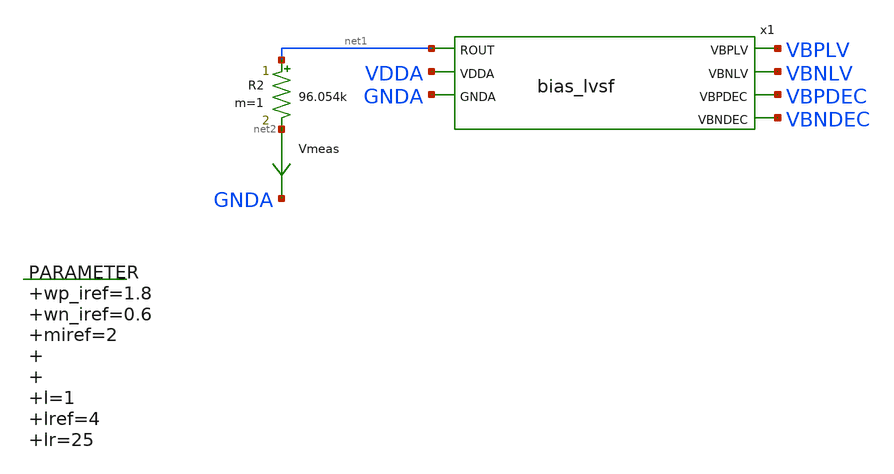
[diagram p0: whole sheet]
** sch_path: xschem/bias_lvsf-tb.sch
.lib $::SKYWATER_MODELS/sky130.lib.spice tt
.include $::SKYWATER_STDCELLS/sky130_fd_sc_hd.spice

**.subckt bias_lvsf-tb
.param wp_iref=1.8 wn_iref=0.6 miref=2 l=1 lref=4 lr=25
R2 net1 net2 96.054k m=1
Vmeas net2 GNDA 0
.save i(vmeas)
x1 net1 VBPLV VBNLV VBPDEC VBNDEC VDDA GNDA bias_lvsf
**** begin user architecture code



  .option wnflag=1
  .option safecurrents
  ***************************STATIC VOLTAGE SOURCE****************************
  Vddh vdda gnd dc 5.5
  VGNDA GNDA gnd 0
  **************************PARAMETERS****************************************
  *.param wsn1=0.6 wsn2=0.6 lx1=5.3 lx2=9.7 lx3=9.2 lx4=4 ws3=1 ws4=1 wsn3=0.64 lx5=12
  .dc R2 80k 120k 1k
  .control
     reset
     save all
     write bias_lvsf-tb.raw
     set wr_singlescale
     set wr_vecnames
     compose wsn1_vec start=0.6 stop=2 step=0.1
     compose wsn2_vec start=0.6 stop=0.7 step=0.01
     compose lx1_vec start=8 stop=15 step=0.1

     *foreach var1 $&wsn2_vec
       *alterparam wsn2=$var1
       reset
       save all
       run
       write bias_lvsf-tb.raw
       set appendwrite
     *end
*    quit 0
  .endc



**** end user architecture code
**.ends

* expanding   symbol:  bias_lvsf.sym # of pins=7
** sym_path: xschem/bias_lvsf.sym
** sch_path: xschem/bias_lvsf.sch
.subckt bias_lvsf ROUT VBPLV VBNLV VBPDEC VBNDEC VDDA GNDA
*.ipin ROUT
*.opin VBPLV
*.opin VBNLV
*.opin VBPDEC
*.opin VBNDEC
*.ipin VDDA
*.ipin GNDA
XM1 n1 n1 VDDA VDDA sky130_fd_pr__pfet_g5v0d10v5 L=lref W=wp_iref nf=1 ad='int((nf+1)/2) * W/nf * 0.29'
+ as='int((nf+2)/2) * W/nf * 0.29' pd='2*int((nf+1)/2) * (W/nf + 0.29)' ps='2*int((nf+2)/2) * (W/nf + 0.29)'
+ nrd='0.29 / W' nrs='0.29 / W' sa=0 sb=0 sd=0 mult=miref m=miref
.param wp_iref=1.8 wn_iref=0.6 miref=2 lref=4 lr=25
XM2 n2 n2 n1 VDDA sky130_fd_pr__pfet_g5v0d10v5 L=lref W=wp_iref nf=1 ad='int((nf+1)/2) * W/nf * 0.29'
+ as='int((nf+2)/2) * W/nf * 0.29' pd='2*int((nf+1)/2) * (W/nf + 0.29)' ps='2*int((nf+2)/2) * (W/nf + 0.29)'
+ nrd='0.29 / W' nrs='0.29 / W' sa=0 sb=0 sd=0 mult=miref m=miref
XR1 ROUT net1 GNDA sky130_fd_pr__res_xhigh_po_5p73 L=0.573 mult=1 m=1
XM3 net2 net1 n2 VDDA sky130_fd_pr__pfet_g5v0d10v5 L=lr W=wp_iref nf=1 ad='int((nf+1)/2) * W/nf * 0.29'
+ as='int((nf+2)/2) * W/nf * 0.29' pd='2*int((nf+1)/2) * (W/nf + 0.29)' ps='2*int((nf+2)/2) * (W/nf + 0.29)'
+ nrd='0.29 / W' nrs='0.29 / W' sa=0 sb=0 sd=0 mult=miref m=miref
XM4 net1 net1 net2 VDDA sky130_fd_pr__pfet_g5v0d10v5 L=lr W=wp_iref nf=1 ad='int((nf+1)/2) * W/nf * 0.29'
+ as='int((nf+2)/2) * W/nf * 0.29' pd='2*int((nf+1)/2) * (W/nf + 0.29)' ps='2*int((nf+2)/2) * (W/nf + 0.29)'
+ nrd='0.29 / W' nrs='0.29 / W' sa=0 sb=0 sd=0 mult=miref m=miref
XM5 net3 n1 VDDA VDDA sky130_fd_pr__pfet_g5v0d10v5 L=lref W=wp_iref nf=1 ad='int((nf+1)/2) * W/nf * 0.29'
+ as='int((nf+2)/2) * W/nf * 0.29' pd='2*int((nf+1)/2) * (W/nf + 0.29)' ps='2*int((nf+2)/2) * (W/nf + 0.29)'
+ nrd='0.29 / W' nrs='0.29 / W' sa=0 sb=0 sd=0 mult=miref m=miref
XM6 n3 n2 net3 VDDA sky130_fd_pr__pfet_g5v0d10v5 L=lref W=wp_iref nf=1 ad='int((nf+1)/2) * W/nf * 0.29'
+ as='int((nf+2)/2) * W/nf * 0.29' pd='2*int((nf+1)/2) * (W/nf + 0.29)' ps='2*int((nf+2)/2) * (W/nf + 0.29)'
+ nrd='0.29 / W' nrs='0.29 / W' sa=0 sb=0 sd=0 mult=miref m=miref
Vmeas1 net8 GNDA 0
.save i(vmeas1)
XM7 n3 n3 n4 GNDA sky130_fd_pr__nfet_g5v0d10v5 L=lref W=wn_iref nf=1 ad='int((nf+1)/2) * W/nf * 0.29'
+ as='int((nf+2)/2) * W/nf * 0.29' pd='2*int((nf+1)/2) * (W/nf + 0.29)' ps='2*int((nf+2)/2) * (W/nf + 0.29)'
+ nrd='0.29 / W' nrs='0.29 / W' sa=0 sb=0 sd=0 mult=miref m=miref
XM8 n4 n4 net8 GNDA sky130_fd_pr__nfet_g5v0d10v5 L=lref W=wn_iref nf=1 ad='int((nf+1)/2) * W/nf * 0.29'
+ as='int((nf+2)/2) * W/nf * 0.29' pd='2*int((nf+1)/2) * (W/nf + 0.29)' ps='2*int((nf+2)/2) * (W/nf + 0.29)'
+ nrd='0.29 / W' nrs='0.29 / W' sa=0 sb=0 sd=0 mult=miref m=miref
XM9 net4 n1 VDDA VDDA sky130_fd_pr__pfet_g5v0d10v5 L=lref W=wp_iref nf=1 ad='int((nf+1)/2) * W/nf * 0.29'
+ as='int((nf+2)/2) * W/nf * 0.29' pd='2*int((nf+1)/2) * (W/nf + 0.29)' ps='2*int((nf+2)/2) * (W/nf + 0.29)'
+ nrd='0.29 / W' nrs='0.29 / W' sa=0 sb=0 sd=0 mult=miref m=miref
XM10 VBNLV n2 net4 VDDA sky130_fd_pr__pfet_g5v0d10v5 L=lref W=wp_iref nf=1 ad='int((nf+1)/2) * W/nf * 0.29'
+ as='int((nf+2)/2) * W/nf * 0.29' pd='2*int((nf+1)/2) * (W/nf + 0.29)' ps='2*int((nf+2)/2) * (W/nf + 0.29)'
+ nrd='0.29 / W' nrs='0.29 / W' sa=0 sb=0 sd=0 mult=miref m=miref
XM11 net5 n1 VDDA VDDA sky130_fd_pr__pfet_g5v0d10v5 L=lref W=wp_iref nf=1 ad='int((nf+1)/2) * W/nf * 0.29'
+ as='int((nf+2)/2) * W/nf * 0.29' pd='2*int((nf+1)/2) * (W/nf + 0.29)' ps='2*int((nf+2)/2) * (W/nf + 0.29)'
+ nrd='0.29 / W' nrs='0.29 / W' sa=0 sb=0 sd=0 mult=miref m=miref
XM12 VBNDEC n2 net5 VDDA sky130_fd_pr__pfet_g5v0d10v5 L=lref W=wp_iref nf=1 ad='int((nf+1)/2) * W/nf * 0.29'
+ as='int((nf+2)/2) * W/nf * 0.29' pd='2*int((nf+1)/2) * (W/nf + 0.29)' ps='2*int((nf+2)/2) * (W/nf + 0.29)'
+ nrd='0.29 / W' nrs='0.29 / W' sa=0 sb=0 sd=0 mult=miref m=miref
XM13 VBNLV VBNLV n6 GNDA sky130_fd_pr__nfet_g5v0d10v5 L=lref W=wn_iref nf=1 ad='int((nf+1)/2) * W/nf * 0.29'
+ as='int((nf+2)/2) * W/nf * 0.29' pd='2*int((nf+1)/2) * (W/nf + 0.29)' ps='2*int((nf+2)/2) * (W/nf + 0.29)'
+ nrd='0.29 / W' nrs='0.29 / W' sa=0 sb=0 sd=0 mult=miref m=miref
XM14 n6 VBNLV net9 GNDA sky130_fd_pr__nfet_g5v0d10v5 L=5.3 W=0.6 nf=1 ad='int((nf+1)/2) * W/nf * 0.29'
+ as='int((nf+2)/2) * W/nf * 0.29' pd='2*int((nf+1)/2) * (W/nf + 0.29)' ps='2*int((nf+2)/2) * (W/nf + 0.29)'
+ nrd='0.29 / W' nrs='0.29 / W' sa=0 sb=0 sd=0 mult=1 m=1
Vmeas2 net9 GNDA 0
.save i(vmeas2)
XM15 VBNDEC VBNDEC n7 GNDA sky130_fd_pr__nfet_g5v0d10v5 L=lref W=wn_iref nf=1 ad='int((nf+1)/2) * W/nf * 0.29'
+ as='int((nf+2)/2) * W/nf * 0.29' pd='2*int((nf+1)/2) * (W/nf + 0.29)' ps='2*int((nf+2)/2) * (W/nf + 0.29)'
+ nrd='0.29 / W' nrs='0.29 / W' sa=0 sb=0 sd=0 mult=miref m=miref
XM16 n7 VBNDEC net10 GNDA sky130_fd_pr__nfet_g5v0d10v5 L=9.7 W=0.61 nf=1 ad='int((nf+1)/2) * W/nf * 0.29'
+ as='int((nf+2)/2) * W/nf * 0.29' pd='2*int((nf+1)/2) * (W/nf + 0.29)' ps='2*int((nf+2)/2) * (W/nf + 0.29)'
+ nrd='0.29 / W' nrs='0.29 / W' sa=0 sb=0 sd=0 mult=1 m=1
Vmeas3 net10 GNDA 0
.save i(vmeas3)
XM17 n10 VBPLV VDDA VDDA sky130_fd_pr__pfet_g5v0d10v5 L=9.2 W=1 nf=1 ad='int((nf+1)/2) * W/nf * 0.29'
+ as='int((nf+2)/2) * W/nf * 0.29' pd='2*int((nf+1)/2) * (W/nf + 0.29)' ps='2*int((nf+2)/2) * (W/nf + 0.29)'
+ nrd='0.29 / W' nrs='0.29 / W' sa=0 sb=0 sd=0 mult=1 m=1
XM18 VBPLV VBPLV n10 VDDA sky130_fd_pr__pfet_g5v0d10v5 L=lref W=wp_iref nf=1 ad='int((nf+1)/2) * W/nf * 0.29'
+ as='int((nf+2)/2) * W/nf * 0.29' pd='2*int((nf+1)/2) * (W/nf + 0.29)' ps='2*int((nf+2)/2) * (W/nf + 0.29)'
+ nrd='0.29 / W' nrs='0.29 / W' sa=0 sb=0 sd=0 mult=miref m=miref
Vmeas4 net11 GNDA 0
.save i(vmeas4)
XM19 VBPLV n3 net6 GNDA sky130_fd_pr__nfet_g5v0d10v5 L=lref W=wn_iref nf=1 ad='int((nf+1)/2) * W/nf * 0.29'
+ as='int((nf+2)/2) * W/nf * 0.29' pd='2*int((nf+1)/2) * (W/nf + 0.29)' ps='2*int((nf+2)/2) * (W/nf + 0.29)'
+ nrd='0.29 / W' nrs='0.29 / W' sa=0 sb=0 sd=0 mult=miref m=miref
XM20 net6 n4 net11 GNDA sky130_fd_pr__nfet_g5v0d10v5 L=lref W=wn_iref nf=1 ad='int((nf+1)/2) * W/nf * 0.29'
+ as='int((nf+2)/2) * W/nf * 0.29' pd='2*int((nf+1)/2) * (W/nf + 0.29)' ps='2*int((nf+2)/2) * (W/nf + 0.29)'
+ nrd='0.29 / W' nrs='0.29 / W' sa=0 sb=0 sd=0 mult=miref m=miref
XM26 net7 n1 VDDA VDDA sky130_fd_pr__pfet_g5v0d10v5 L=lref W=wp_iref nf=1 ad='int((nf+1)/2) * W/nf * 0.29'
+ as='int((nf+2)/2) * W/nf * 0.29' pd='2*int((nf+1)/2) * (W/nf + 0.29)' ps='2*int((nf+2)/2) * (W/nf + 0.29)'
+ nrd='0.29 / W' nrs='0.29 / W' sa=0 sb=0 sd=0 mult=miref m=miref
XM27 VBPDEC n2 net7 VDDA sky130_fd_pr__pfet_g5v0d10v5 L=lref W=wp_iref nf=1 ad='int((nf+1)/2) * W/nf * 0.29'
+ as='int((nf+2)/2) * W/nf * 0.29' pd='2*int((nf+1)/2) * (W/nf + 0.29)' ps='2*int((nf+2)/2) * (W/nf + 0.29)'
+ nrd='0.29 / W' nrs='0.29 / W' sa=0 sb=0 sd=0 mult=miref m=miref
XM28 VBPDEC VBPDEC n14 GNDA sky130_fd_pr__nfet_g5v0d10v5 L=lref W=wn_iref nf=1 ad='int((nf+1)/2) * W/nf * 0.29'
+ as='int((nf+2)/2) * W/nf * 0.29' pd='2*int((nf+1)/2) * (W/nf + 0.29)' ps='2*int((nf+2)/2) * (W/nf + 0.29)'
+ nrd='0.29 / W' nrs='0.29 / W' sa=0 sb=0 sd=0 mult=miref m=miref
XM29 n14 n14 net12 GNDA sky130_fd_pr__nfet_g5v0d10v5 L=12 W=0.64 nf=1 ad='int((nf+1)/2) * W/nf * 0.29'
+ as='int((nf+2)/2) * W/nf * 0.29' pd='2*int((nf+1)/2) * (W/nf + 0.29)' ps='2*int((nf+2)/2) * (W/nf + 0.29)'
+ nrd='0.29 / W' nrs='0.29 / W' sa=0 sb=0 sd=0 mult=1 m=1
Vmeas6 net12 GNDA 0
.save i(vmeas6)
.ends

.end
